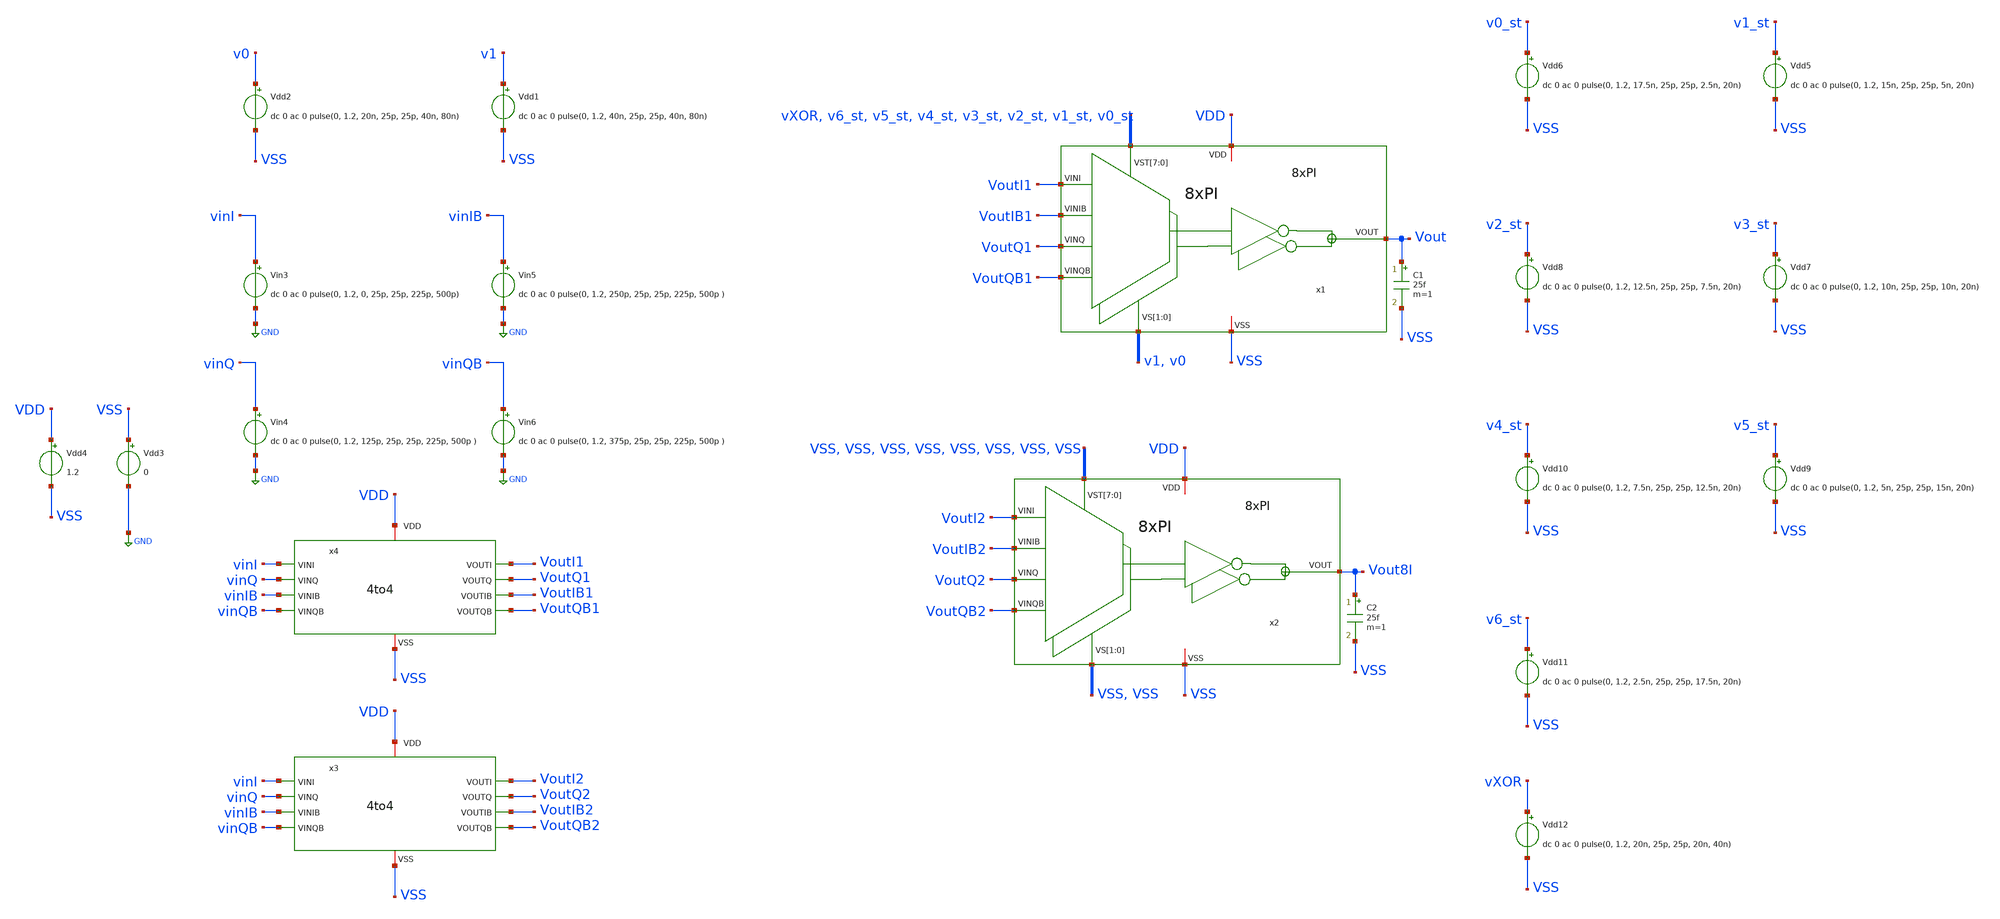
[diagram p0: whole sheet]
** sch_path: CDR4176-main/testbenches/tran/xschem/tb_linearity_8xPI_top.sch
**.subckt tb_linearity_8xPI_top
Vin3 vinI GND dc 0 ac 0 pulse(0, 1.2, 0, 25p, 25p, 225p, 500p)
Vin4 vinQ GND dc 0 ac 0 pulse(0, 1.2, 125p, 25p, 25p, 225p, 500p )
Vin5 vinIB GND dc 0 ac 0 pulse(0, 1.2, 250p, 25p, 25p, 225p, 500p )
Vin6 vinQB GND dc 0 ac 0 pulse(0, 1.2, 375p, 25p, 25p, 225p, 500p )
x4 VDD vinI VoutI1 VoutQ1 vinQ vinIB VoutIB1 vinQB VoutQB1 VSS 4to4
Vdd4 VDD VSS 1.2
Vdd1 v1 VSS dc 0 ac 0 pulse(0, 1.2, 40n, 25p, 25p, 40n, 80n)
Vdd2 v0 VSS dc 0 ac 0 pulse(0, 1.2, 20n, 25p, 25p, 40n, 80n)
Vdd3 VSS GND 0
x1 VoutI1 VoutIB1 VoutQ1 VoutQB1 v1 v0 vXOR v6_st v5_st v4_st v3_st v2_st v1_st v0_st Vout VDD VSS
+ 8xPI
C1 Vout VSS 25f m=1
x2 VoutI2 VoutIB2 VoutQ2 VoutQB2 VSS VSS VSS VSS VSS VSS VSS VSS VSS VSS Vout8I VDD VSS 8xPI
C2 Vout8I VSS 25f m=1
Vdd5 v1_st VSS dc 0 ac 0 pulse(0, 1.2, 15n, 25p, 25p, 5n, 20n)
Vdd6 v0_st VSS dc 0 ac 0 pulse(0, 1.2, 17.5n, 25p, 25p, 2.5n, 20n)
Vdd7 v3_st VSS dc 0 ac 0 pulse(0, 1.2, 10n, 25p, 25p, 10n, 20n)
Vdd8 v2_st VSS dc 0 ac 0 pulse(0, 1.2, 12.5n, 25p, 25p, 7.5n, 20n)
Vdd9 v5_st VSS dc 0 ac 0 pulse(0, 1.2, 5n, 25p, 25p, 15n, 20n)
Vdd10 v4_st VSS dc 0 ac 0 pulse(0, 1.2, 7.5n, 25p, 25p, 12.5n, 20n)
Vdd11 v6_st VSS dc 0 ac 0 pulse(0, 1.2, 2.5n, 25p, 25p, 17.5n, 20n)
x3 VDD vinI VoutI2 VoutQ2 vinQ vinIB VoutIB2 vinQB VoutQB2 VSS 4to4
Vdd12 vXOR VSS dc 0 ac 0 pulse(0, 1.2, 20n, 25p, 25p, 20n, 40n)
**** begin user architecture code



* Circuit Parameters
.param vdd = 1.2
.param vss = 0.0
.param a=0
.param b=0
.param c=0
.param d=1
.param Tclk = 500P
.options TEMP = 27.0

* Include Models
*.lib /opt/pdks/ihp-sg13g2/libs.tech/ngspice/models/cornerMOSlv.lib mos_tt
*.lib /opt/pdks/ihp-sg13g2/libs.tech/ngspice/models/cornerMOShv.lib mos_tt
*.lib /opt/pdks/ihp-sg13g2/libs.tech/ngspice/models/cornerHBT.lib hbt_typ
*.lib /opt/pdks/ihp-sg13g2/libs.tech/ngspice/models/cornerRES.lib res_typ
.lib cornerMOSlv.lib mos_tt


* OP Parameters & Singals to save
.save V(Vout) V(Vout8I) V(vinI) V(VoutI1) V(VoutI2) V(VoutQ1) V(VoutIB1) V(VoutQB1)

*Simulations
.control
*set output_path = tb_linearity_8xpi/
	tran 5PS 80NS
	*setplot tran1
	*plot v0 v1+1.5 v0_st+3 v6_st+4.5 Vout+6 Vout8I+7.5 ylabel vout xlabel vin
	set filetype = ascii
        write tran_linearity_termoless.raw V(Vout) V(Vout8I) V(vinI) V(VoutI1) V(VoutI2) V(VoutQ1)
+ V(VoutIB1) V(VoutQB1)
	*write {$output_path}tran_linearity_termoless.raw V(Vout) V(Vout8I) V(vinI) V(VoutI1) V(VoutI2) V(VoutQ1)
+ V(VoutIB1) V(VoutQB1)
.endc
.end

**** end user architecture code
**.ends
.GLOBAL GND
.end
